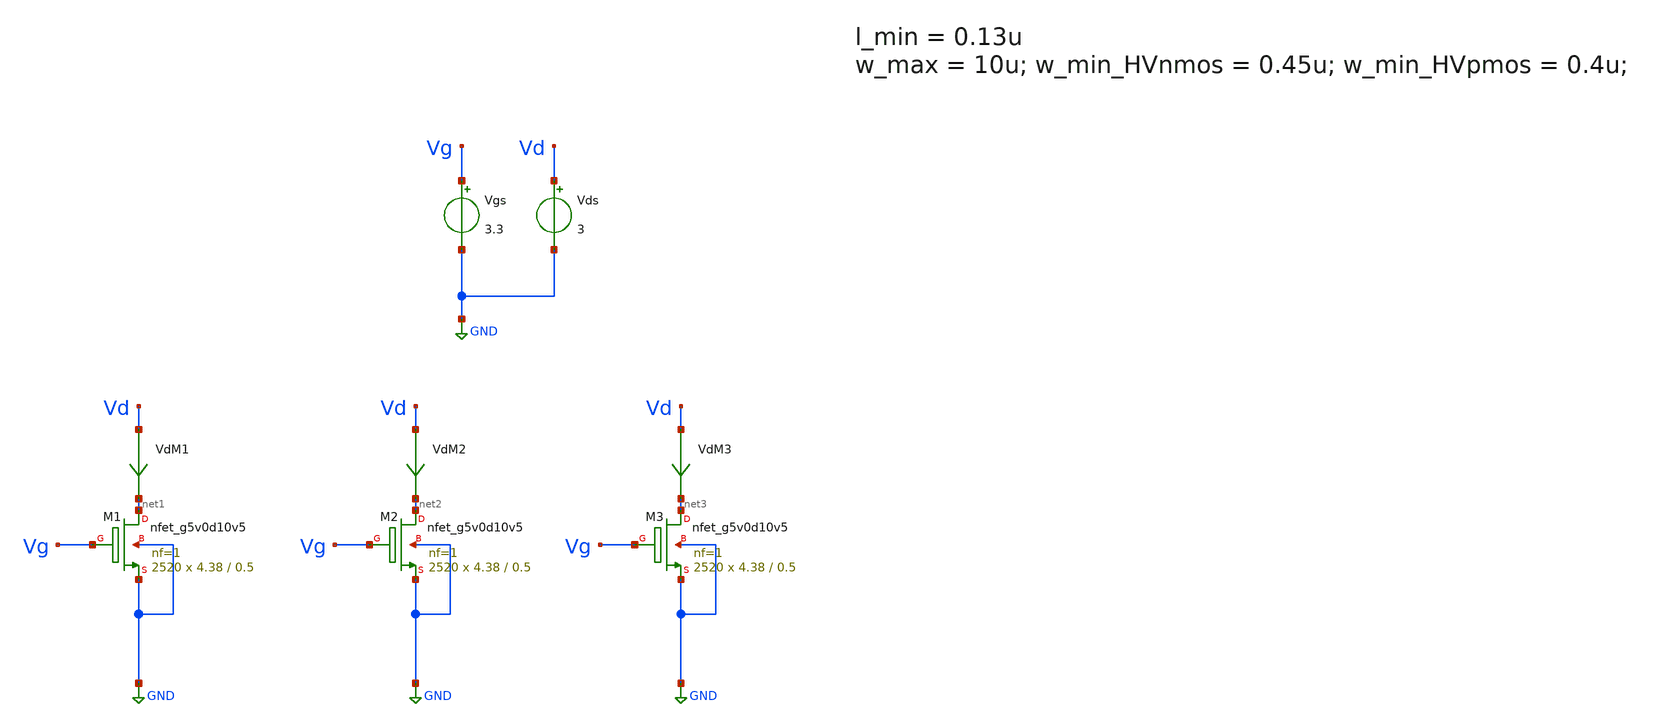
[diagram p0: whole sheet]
** sch_path: xschem/TB_hvNMOS_charact_SKY130.sch
.lib $::SKYWATER_MODELS/sky130.lib.spice tt
.include $::SKYWATER_STDCELLS/sky130_fd_sc_hd.spice

**.subckt TB_hvNMOS_charact_SKY130
Vgs Vg GND 3.3
Vds Vd GND 3
VdM1 Vd net1 0
.save i(vdm1)
VdM2 Vd net2 0
.save i(vdm2)
VdM3 Vd net3 0
.save i(vdm3)
XM1 net1 Vg GND GND sky130_fd_pr__nfet_g5v0d10v5 L=0.5 W=4.38 nf=1 ad='int((nf+1)/2) * W/nf * 0.29' as='int((nf+2)/2) * W/nf * 0.29'
+ pd='2*int((nf+1)/2) * (W/nf + 0.29)' ps='2*int((nf+2)/2) * (W/nf + 0.29)' nrd='0.29 / W' nrs='0.29 / W'
+ sa=0 sb=0 sd=0 mult=2520 m=2520
XM2 net2 Vg GND GND sky130_fd_pr__nfet_g5v0d10v5 L=0.5 W=4.38 nf=1 ad='int((nf+1)/2) * W/nf * 0.29' as='int((nf+2)/2) * W/nf * 0.29'
+ pd='2*int((nf+1)/2) * (W/nf + 0.29)' ps='2*int((nf+2)/2) * (W/nf + 0.29)' nrd='0.29 / W' nrs='0.29 / W'
+ sa=0 sb=0 sd=0 mult=2520 m=2520
XM3 net3 Vg GND GND sky130_fd_pr__nfet_g5v0d10v5 L=0.5 W=4.38 nf=1 ad='int((nf+1)/2) * W/nf * 0.29' as='int((nf+2)/2) * W/nf * 0.29'
+ pd='2*int((nf+1)/2) * (W/nf + 0.29)' ps='2*int((nf+2)/2) * (W/nf + 0.29)' nrd='0.29 / W' nrs='0.29 / W'
+ sa=0 sb=0 sd=0 mult=2520 m=2520
**** begin user architecture code


.param temp=27
.param mult_M1 = 1200
.param w_M1 =10u
.param l_M1 =0.22u

.param mult_M2 = 1200
.param w_M2 =10u
.param l_M2 =0.25u

.param mult_M3 = 1200
.param w_M3 =10u
.param l_M3 =0.35u

.save all
* + @M.XM1.m1[id]  @m.xm2.msky130_fd_pr__nfet_g5v0d10v5[vth]
*+  @m.xm1.msky130_fd_pr__nfet_g5v0d10v5[gds]  @m.xm2.msky130_fd_pr__nfet_g5v0d10v5[vth]  @m.xm2.msky130_fd_pr__nfet_g5v0d10v5[gds]
*+  @m.xm3.msky130_fd_pr__nfet_g5v0d10v5[vth]  @m.xm3.msky130_fd_pr__nfet_g5v0d10v5[gds]  @m.xm1.msky130_fd_pr__nfet_g5v0d10v5[ad]

.control
*dc Vds 0 3 0.01 Vgs 0.5 3 0.5
dc Vds 0 3 0.01
*dc Vds 0 0.5 0.01
*dc Vds 0 0.5 0.01 temp 0 27 1
write dc_hv_nmos.raw
let G_M1 = @m.xm1.msky130_fd_pr__nfet_g5v0d10v5[gds]
let G_M2 = @m.xm2.msky130_fd_pr__nfet_g5v0d10v5[gds]
let G_M3 = @m.xm3.msky130_fd_pr__nfet_g5v0d10v5[gds]
let Ron_M1 = 1/G_M1
let Ron_M2 = 1/G_M2
let Ron_M3 = 1/G_M3
let Vds = v(Vd)

let Vth_M1 = @m.xm1.msky130_fd_pr__nfet_g5v0d10v5[vth]
let Id_M1 = i(VdM1)
plot i(VdM1) i(VdM2) i(VdM3) vs Vds
plot Ron_M1 Ron_M2 Ron_M3 vs Vds
*plot Id_M1
*plot Vth_M1 Vth_M1*2
*print @n.xm1.nsg13_hv_nmos[vth] @n.xm2.nsg13_hv_nmos[vth] Vth_M1
*print @n.xm2.nsg13_hv_nmos[vth]
write test_nmos.raw




.endc


**** end user architecture code
**.ends
.GLOBAL GND
.end
